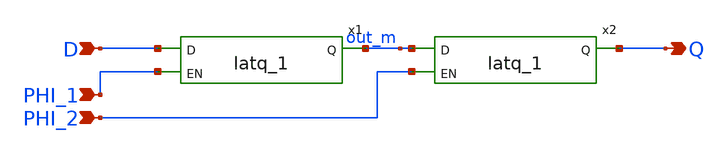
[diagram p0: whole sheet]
** sch_path: designs/untitled.sch
**.subckt untitled D PHI_1 PHI_2 Q
*.ipin D
*.ipin PHI_1
*.ipin PHI_2
*.opin Q
x1 D PHI_1 out_m VDDd VDDd VSSd VSSd gf180mcu_fd_sc_mcu9t5v0__latq_1
x2 out_m PHI_2 Q VDDd VDDd VSSd VSSd gf180mcu_fd_sc_mcu9t5v0__latq_1
**.ends
.end
